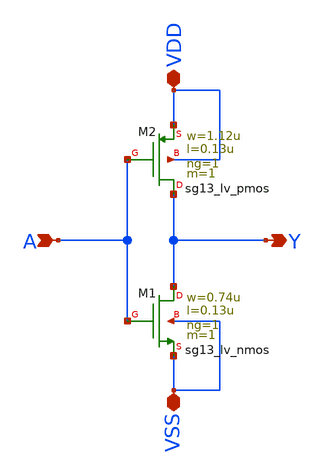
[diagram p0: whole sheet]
** sch_path: _tests/23/ihp-sg13cmos5l/inv.sch
**.subckt inv A Y VDD VSS
*.ipin A
*.opin Y
*.iopin VDD
*.iopin VSS
XM1 Y A VSS VSS sg13_lv_nmos w=0.74u l=0.13u ng=1 m=1 mm_ok=1
XM2 Y A VDD VDD sg13_lv_pmos w=1.12u l=0.13u ng=1 m=1 mm_ok=1
**.ends
.end
